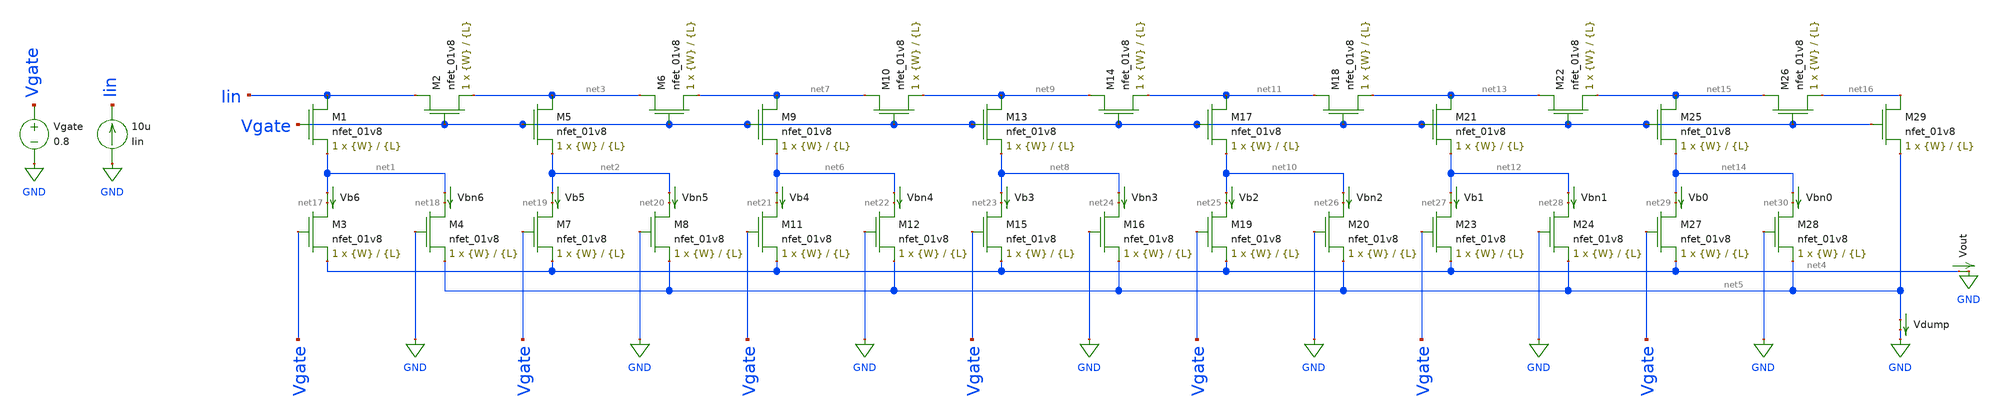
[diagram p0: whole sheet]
** sch_path: schematics/dac_from_paper.sch
**.subckt dac_from_paper
XM1 Iin Vgate net1 GND sky130_fd_pr__nfet_01v8 L={L} W={W} nf=1 ad='int((nf+1)/2) * W/nf * 0.29' as='int((nf+2)/2) * W/nf * 0.29'
+ pd='2*int((nf+1)/2) * (W/nf + 0.29)' ps='2*int((nf+2)/2) * (W/nf + 0.29)' nrd='0.29 / W' nrs='0.29 / W'
+ sa=0 sb=0 sd=0 mult=1 m=1
XM2 Iin Vgate net3 GND sky130_fd_pr__nfet_01v8 L={L} W={W} nf=1 ad='int((nf+1)/2) * W/nf * 0.29' as='int((nf+2)/2) * W/nf * 0.29'
+ pd='2*int((nf+1)/2) * (W/nf + 0.29)' ps='2*int((nf+2)/2) * (W/nf + 0.29)' nrd='0.29 / W' nrs='0.29 / W'
+ sa=0 sb=0 sd=0 mult=1 m=1
XM3 net17 Vgate net4 GND sky130_fd_pr__nfet_01v8 L={L} W={W} nf=1 ad='int((nf+1)/2) * W/nf * 0.29' as='int((nf+2)/2) * W/nf * 0.29'
+ pd='2*int((nf+1)/2) * (W/nf + 0.29)' ps='2*int((nf+2)/2) * (W/nf + 0.29)' nrd='0.29 / W' nrs='0.29 / W'
+ sa=0 sb=0 sd=0 mult=1 m=1
XM4 net18 GND net5 GND sky130_fd_pr__nfet_01v8 L={L} W={W} nf=1 ad='int((nf+1)/2) * W/nf * 0.29' as='int((nf+2)/2) * W/nf * 0.29'
+ pd='2*int((nf+1)/2) * (W/nf + 0.29)' ps='2*int((nf+2)/2) * (W/nf + 0.29)' nrd='0.29 / W' nrs='0.29 / W'
+ sa=0 sb=0 sd=0 mult=1 m=1
XM5 net3 Vgate net2 GND sky130_fd_pr__nfet_01v8 L={L} W={W} nf=1 ad='int((nf+1)/2) * W/nf * 0.29' as='int((nf+2)/2) * W/nf * 0.29'
+ pd='2*int((nf+1)/2) * (W/nf + 0.29)' ps='2*int((nf+2)/2) * (W/nf + 0.29)' nrd='0.29 / W' nrs='0.29 / W'
+ sa=0 sb=0 sd=0 mult=1 m=1
XM6 net3 Vgate net7 GND sky130_fd_pr__nfet_01v8 L={L} W={W} nf=1 ad='int((nf+1)/2) * W/nf * 0.29' as='int((nf+2)/2) * W/nf * 0.29'
+ pd='2*int((nf+1)/2) * (W/nf + 0.29)' ps='2*int((nf+2)/2) * (W/nf + 0.29)' nrd='0.29 / W' nrs='0.29 / W'
+ sa=0 sb=0 sd=0 mult=1 m=1
XM7 net19 Vgate net4 GND sky130_fd_pr__nfet_01v8 L={L} W={W} nf=1 ad='int((nf+1)/2) * W/nf * 0.29' as='int((nf+2)/2) * W/nf * 0.29'
+ pd='2*int((nf+1)/2) * (W/nf + 0.29)' ps='2*int((nf+2)/2) * (W/nf + 0.29)' nrd='0.29 / W' nrs='0.29 / W'
+ sa=0 sb=0 sd=0 mult=1 m=1
XM8 net20 GND net5 GND sky130_fd_pr__nfet_01v8 L={L} W={W} nf=1 ad='int((nf+1)/2) * W/nf * 0.29' as='int((nf+2)/2) * W/nf * 0.29'
+ pd='2*int((nf+1)/2) * (W/nf + 0.29)' ps='2*int((nf+2)/2) * (W/nf + 0.29)' nrd='0.29 / W' nrs='0.29 / W'
+ sa=0 sb=0 sd=0 mult=1 m=1
XM9 net7 Vgate net6 GND sky130_fd_pr__nfet_01v8 L={L} W={W} nf=1 ad='int((nf+1)/2) * W/nf * 0.29' as='int((nf+2)/2) * W/nf * 0.29'
+ pd='2*int((nf+1)/2) * (W/nf + 0.29)' ps='2*int((nf+2)/2) * (W/nf + 0.29)' nrd='0.29 / W' nrs='0.29 / W'
+ sa=0 sb=0 sd=0 mult=1 m=1
XM10 net7 Vgate net9 GND sky130_fd_pr__nfet_01v8 L={L} W={W} nf=1 ad='int((nf+1)/2) * W/nf * 0.29' as='int((nf+2)/2) * W/nf * 0.29'
+ pd='2*int((nf+1)/2) * (W/nf + 0.29)' ps='2*int((nf+2)/2) * (W/nf + 0.29)' nrd='0.29 / W' nrs='0.29 / W'
+ sa=0 sb=0 sd=0 mult=1 m=1
XM11 net21 Vgate net4 GND sky130_fd_pr__nfet_01v8 L={L} W={W} nf=1 ad='int((nf+1)/2) * W/nf * 0.29' as='int((nf+2)/2) * W/nf * 0.29'
+ pd='2*int((nf+1)/2) * (W/nf + 0.29)' ps='2*int((nf+2)/2) * (W/nf + 0.29)' nrd='0.29 / W' nrs='0.29 / W'
+ sa=0 sb=0 sd=0 mult=1 m=1
XM12 net22 GND net5 GND sky130_fd_pr__nfet_01v8 L={L} W={W} nf=1 ad='int((nf+1)/2) * W/nf * 0.29' as='int((nf+2)/2) * W/nf * 0.29'
+ pd='2*int((nf+1)/2) * (W/nf + 0.29)' ps='2*int((nf+2)/2) * (W/nf + 0.29)' nrd='0.29 / W' nrs='0.29 / W'
+ sa=0 sb=0 sd=0 mult=1 m=1
XM13 net9 Vgate net8 GND sky130_fd_pr__nfet_01v8 L={L} W={W} nf=1 ad='int((nf+1)/2) * W/nf * 0.29' as='int((nf+2)/2) * W/nf * 0.29'
+ pd='2*int((nf+1)/2) * (W/nf + 0.29)' ps='2*int((nf+2)/2) * (W/nf + 0.29)' nrd='0.29 / W' nrs='0.29 / W'
+ sa=0 sb=0 sd=0 mult=1 m=1
XM14 net9 Vgate net11 GND sky130_fd_pr__nfet_01v8 L={L} W={W} nf=1 ad='int((nf+1)/2) * W/nf * 0.29' as='int((nf+2)/2) * W/nf * 0.29'
+ pd='2*int((nf+1)/2) * (W/nf + 0.29)' ps='2*int((nf+2)/2) * (W/nf + 0.29)' nrd='0.29 / W' nrs='0.29 / W'
+ sa=0 sb=0 sd=0 mult=1 m=1
XM15 net23 Vgate net4 GND sky130_fd_pr__nfet_01v8 L={L} W={W} nf=1 ad='int((nf+1)/2) * W/nf * 0.29' as='int((nf+2)/2) * W/nf * 0.29'
+ pd='2*int((nf+1)/2) * (W/nf + 0.29)' ps='2*int((nf+2)/2) * (W/nf + 0.29)' nrd='0.29 / W' nrs='0.29 / W'
+ sa=0 sb=0 sd=0 mult=1 m=1
XM16 net24 GND net5 GND sky130_fd_pr__nfet_01v8 L={L} W={W} nf=1 ad='int((nf+1)/2) * W/nf * 0.29' as='int((nf+2)/2) * W/nf * 0.29'
+ pd='2*int((nf+1)/2) * (W/nf + 0.29)' ps='2*int((nf+2)/2) * (W/nf + 0.29)' nrd='0.29 / W' nrs='0.29 / W'
+ sa=0 sb=0 sd=0 mult=1 m=1
XM17 net11 Vgate net10 GND sky130_fd_pr__nfet_01v8 L={L} W={W} nf=1 ad='int((nf+1)/2) * W/nf * 0.29'
+ as='int((nf+2)/2) * W/nf * 0.29' pd='2*int((nf+1)/2) * (W/nf + 0.29)' ps='2*int((nf+2)/2) * (W/nf + 0.29)'
+ nrd='0.29 / W' nrs='0.29 / W' sa=0 sb=0 sd=0 mult=1 m=1
XM18 net11 Vgate net13 GND sky130_fd_pr__nfet_01v8 L={L} W={W} nf=1 ad='int((nf+1)/2) * W/nf * 0.29'
+ as='int((nf+2)/2) * W/nf * 0.29' pd='2*int((nf+1)/2) * (W/nf + 0.29)' ps='2*int((nf+2)/2) * (W/nf + 0.29)'
+ nrd='0.29 / W' nrs='0.29 / W' sa=0 sb=0 sd=0 mult=1 m=1
XM19 net25 Vgate net4 GND sky130_fd_pr__nfet_01v8 L={L} W={W} nf=1 ad='int((nf+1)/2) * W/nf * 0.29' as='int((nf+2)/2) * W/nf * 0.29'
+ pd='2*int((nf+1)/2) * (W/nf + 0.29)' ps='2*int((nf+2)/2) * (W/nf + 0.29)' nrd='0.29 / W' nrs='0.29 / W'
+ sa=0 sb=0 sd=0 mult=1 m=1
XM20 net26 GND net5 GND sky130_fd_pr__nfet_01v8 L={L} W={W} nf=1 ad='int((nf+1)/2) * W/nf * 0.29' as='int((nf+2)/2) * W/nf * 0.29'
+ pd='2*int((nf+1)/2) * (W/nf + 0.29)' ps='2*int((nf+2)/2) * (W/nf + 0.29)' nrd='0.29 / W' nrs='0.29 / W'
+ sa=0 sb=0 sd=0 mult=1 m=1
XM21 net13 Vgate net12 GND sky130_fd_pr__nfet_01v8 L={L} W={W} nf=1 ad='int((nf+1)/2) * W/nf * 0.29'
+ as='int((nf+2)/2) * W/nf * 0.29' pd='2*int((nf+1)/2) * (W/nf + 0.29)' ps='2*int((nf+2)/2) * (W/nf + 0.29)'
+ nrd='0.29 / W' nrs='0.29 / W' sa=0 sb=0 sd=0 mult=1 m=1
XM22 net13 Vgate net15 GND sky130_fd_pr__nfet_01v8 L={L} W={W} nf=1 ad='int((nf+1)/2) * W/nf * 0.29'
+ as='int((nf+2)/2) * W/nf * 0.29' pd='2*int((nf+1)/2) * (W/nf + 0.29)' ps='2*int((nf+2)/2) * (W/nf + 0.29)'
+ nrd='0.29 / W' nrs='0.29 / W' sa=0 sb=0 sd=0 mult=1 m=1
XM23 net27 Vgate net4 GND sky130_fd_pr__nfet_01v8 L={L} W={W} nf=1 ad='int((nf+1)/2) * W/nf * 0.29' as='int((nf+2)/2) * W/nf * 0.29'
+ pd='2*int((nf+1)/2) * (W/nf + 0.29)' ps='2*int((nf+2)/2) * (W/nf + 0.29)' nrd='0.29 / W' nrs='0.29 / W'
+ sa=0 sb=0 sd=0 mult=1 m=1
XM24 net28 GND net5 GND sky130_fd_pr__nfet_01v8 L={L} W={W} nf=1 ad='int((nf+1)/2) * W/nf * 0.29' as='int((nf+2)/2) * W/nf * 0.29'
+ pd='2*int((nf+1)/2) * (W/nf + 0.29)' ps='2*int((nf+2)/2) * (W/nf + 0.29)' nrd='0.29 / W' nrs='0.29 / W'
+ sa=0 sb=0 sd=0 mult=1 m=1
XM25 net15 Vgate net14 GND sky130_fd_pr__nfet_01v8 L={L} W={W} nf=1 ad='int((nf+1)/2) * W/nf * 0.29'
+ as='int((nf+2)/2) * W/nf * 0.29' pd='2*int((nf+1)/2) * (W/nf + 0.29)' ps='2*int((nf+2)/2) * (W/nf + 0.29)'
+ nrd='0.29 / W' nrs='0.29 / W' sa=0 sb=0 sd=0 mult=1 m=1
XM26 net15 Vgate net16 GND sky130_fd_pr__nfet_01v8 L={L} W={W} nf=1 ad='int((nf+1)/2) * W/nf * 0.29'
+ as='int((nf+2)/2) * W/nf * 0.29' pd='2*int((nf+1)/2) * (W/nf + 0.29)' ps='2*int((nf+2)/2) * (W/nf + 0.29)'
+ nrd='0.29 / W' nrs='0.29 / W' sa=0 sb=0 sd=0 mult=1 m=1
XM27 net29 Vgate net4 GND sky130_fd_pr__nfet_01v8 L={L} W={W} nf=1 ad='int((nf+1)/2) * W/nf * 0.29' as='int((nf+2)/2) * W/nf * 0.29'
+ pd='2*int((nf+1)/2) * (W/nf + 0.29)' ps='2*int((nf+2)/2) * (W/nf + 0.29)' nrd='0.29 / W' nrs='0.29 / W'
+ sa=0 sb=0 sd=0 mult=1 m=1
XM28 net30 GND net5 GND sky130_fd_pr__nfet_01v8 L={L} W={W} nf=1 ad='int((nf+1)/2) * W/nf * 0.29' as='int((nf+2)/2) * W/nf * 0.29'
+ pd='2*int((nf+1)/2) * (W/nf + 0.29)' ps='2*int((nf+2)/2) * (W/nf + 0.29)' nrd='0.29 / W' nrs='0.29 / W'
+ sa=0 sb=0 sd=0 mult=1 m=1
XM29 net16 Vgate net5 GND sky130_fd_pr__nfet_01v8 L={L} W={W} nf=1 ad='int((nf+1)/2) * W/nf * 0.29' as='int((nf+2)/2) * W/nf * 0.29'
+ pd='2*int((nf+1)/2) * (W/nf + 0.29)' ps='2*int((nf+2)/2) * (W/nf + 0.29)' nrd='0.29 / W' nrs='0.29 / W'
+ sa=0 sb=0 sd=0 mult=1 m=1
Vdump net5 GND 0
.save i(vdump)
Vgate Vgate GND 0.8
Vb0 net14 net29 0
.save i(vb0)
Vbn0 net14 net30 0
.save i(vbn0)
Vb5 net2 net19 0
.save i(vb5)
Vb6 net1 net17 0
.save i(vb6)
Iin GND Iin 10u
Vout net4 GND 0
.save i(vout)
Vb1 net12 net27 0
.save i(vb1)
Vb2 net10 net25 0
.save i(vb2)
Vb3 net8 net23 0
.save i(vb3)
Vb4 net6 net21 0
.save i(vb4)
Vbn1 net12 net28 0
.save i(vbn1)
Vbn2 net10 net26 0
.save i(vbn2)
Vbn3 net8 net24 0
.save i(vbn3)
Vbn4 net6 net22 0
.save i(vbn4)
Vbn5 net2 net20 0
.save i(vbn5)
Vbn6 net1 net18 0
.save i(vbn6)
**** begin user architecture code

.option wnflag=1
.param MC_SWITCH=0.0
.lib ~/skywater/skywater-pdk/libraries/sky130_fd_pr_ngspice/latest/models/sky130.lib.spice tt


.param W=1
.param L=0.5
.control
tran 1u 100u
save all
run
plot i(Vb6) i(Vb5) i(Vb4) i(Vb3) i(Vb2) i(Vb1) i(Vb0) i(Vout)
.endc

**** end user architecture code
**.ends
.GLOBAL GND
.end
